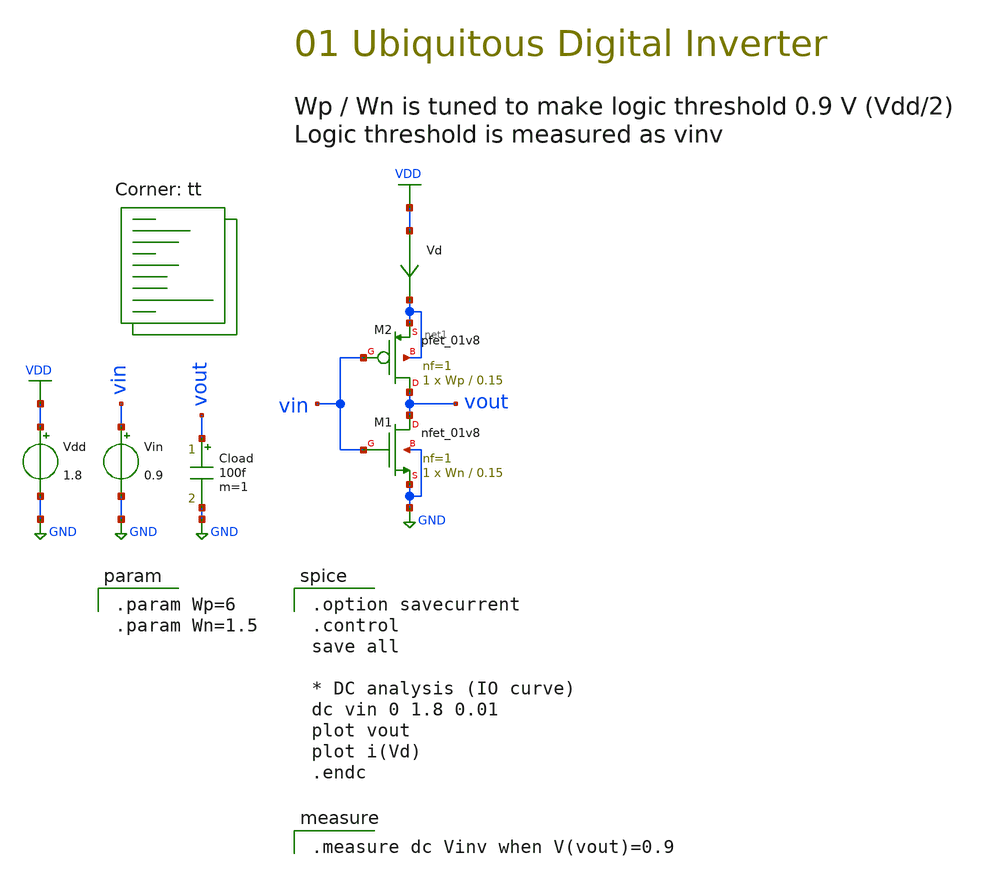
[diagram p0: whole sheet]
** sch_path: 01-a_inverter.sch
**.subckt 01-a_inverter
Vdd VDD GND 1.8
Vin vin GND 0.9
XM2 vout vin net1 net1 sky130_fd_pr__pfet_01v8 L=0.15 W=Wp nf=1 ad='int((nf+1)/2) * W/nf * 0.29' as='int((nf+2)/2) * W/nf * 0.29'
+ pd='2*int((nf+1)/2) * (W/nf + 0.29)' ps='2*int((nf+2)/2) * (W/nf + 0.29)' nrd='0.29 / W' nrs='0.29 / W'
+ sa=0 sb=0 sd=0 mult=1 m=1
XM1 vout vin GND GND sky130_fd_pr__nfet_01v8 L=0.15 W=Wn nf=1 ad='int((1 + 1)/2) * Wn / 1 * 0.29' as='int((1 + 2)/2) * Wn / 1 * 0.29'
+ pd='2*int((1 + 1)/2) * (Wn / 1 + 0.29)' ps='2*int((1 + 2)/2) * (Wn / 1 + 0.29)' nrd='0.29 / Wn ' nrs='0.29 / Wn '
+ sa=0 sb=0 sd=0 mult=1 m=1
Vd VDD net1 0
.save i(vd)
Cload vout GND 100f m=1
**** begin user architecture code
.lib $::SKYWATER_MODELS/sky130.lib.spice tt

.param Wp=6
.param Wn=1.5


.option savecurrent
.control
save all

* DC analysis (IO curve)
dc vin 0 1.8 0.01
plot vout
plot i(Vd)
.endc


.measure dc Vinv when V(vout)=0.9

**** end user architecture code
**.ends
.GLOBAL GND
.GLOBAL VDD
.end
